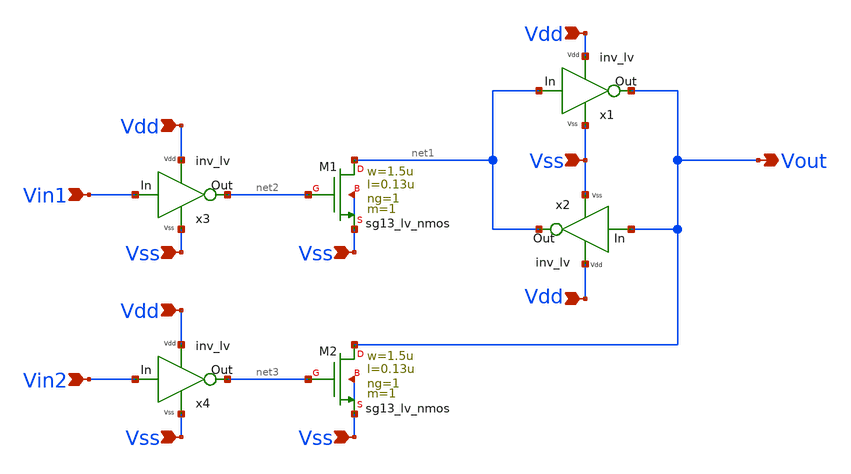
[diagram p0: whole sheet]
** sch_path: xschem/sch/inv_latch.sch
**.subckt inv_latch Vout Vdd Vdd Vin1 Vss Vss Vdd Vss Vdd Vin2 Vss Vss
*.opin Vout
*.ipin Vdd
*.ipin Vdd
*.ipin Vin1
*.ipin Vss
*.ipin Vss
*.ipin Vdd
*.ipin Vss
*.ipin Vdd
*.ipin Vin2
*.ipin Vss
*.ipin Vss
x1 net1 Vout Vdd Vss inv_lv
x2 Vout net1 Vdd Vss inv_lv
XM1 net1 net2 Vss Vss sg13_lv_nmos w=1.5u l=0.13u ng=1 m=1 mm_ok=1
x3 Vin1 net2 Vdd Vss inv_lv
XM2 Vout net3 Vss Vss sg13_lv_nmos w=1.5u l=0.13u ng=1 m=1 mm_ok=1
x4 Vin2 net3 Vdd Vss inv_lv
**.ends

* expanding   symbol:
*+  /workspaces/usm-vlsi-tools/shared_xserver/proyecto-IPD413/xschem/sch/inv_lv.sym # of pins=4
** sym_path: xschem/sch/inv_lv.sym
** sch_path: xschem/sch/inv_lv.sch
.subckt inv_lv Vin Vout Vdd Vss
*.ipin Vdd
*.ipin Vss
*.ipin Vin
*.opin Vout
XM1 Vss Vin Vout Vss sg13_lv_nmos w=1u l=0.13u ng=1 m=1 mm_ok=1
XM2 Vout Vin Vdd Vdd sg13_lv_pmos w=2.3u l=0.13u ng=1 m=1 mm_ok=1
.ends

.end
